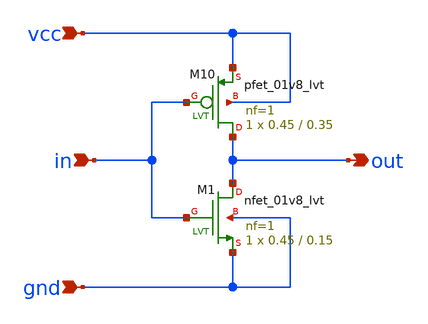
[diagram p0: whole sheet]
** sch_path: Oscillators/Ring-Oscillator/delay_cell.sch
**.subckt delay_cell vcc gnd in out
*.ipin vcc
*.ipin gnd
*.ipin in
*.opin out
XM1 out in gnd gnd sky130_fd_pr__nfet_01v8_lvt L=0.15 W=0.45 nf=1 ad='int((1 + 1)/2) * 0.45 / 1 * 0.29'
+ as='int((1 + 2)/2) * 0.45 / 1 * 0.29' pd='2*int((1 + 1)/2) * (0.45 / 1 + 0.29)' ps='2*int((1 + 2)/2) * (0.45 / 1 + 0.29)'
+ nrd='0.29 / 0.45 ' nrs='0.29 / 0.45 ' sa=0 sb=0 sd=0 mult=1 m=1
XM10 out in vcc vcc sky130_fd_pr__pfet_01v8_lvt L=0.35 W=0.45 nf=1 ad='int((1 + 1)/2) * 0.45 / 1 * 0.29'
+ as='int((1 + 2)/2) * 0.45 / 1 * 0.29' pd='2*int((1 + 1)/2) * (0.45 / 1 + 0.29)' ps='2*int((1 + 2)/2) * (0.45 / 1 + 0.29)'
+ nrd='0.29 / 0.45 ' nrs='0.29 / 0.45 ' sa=0 sb=0 sd=0 mult=1 m=1
**.ends
.end
